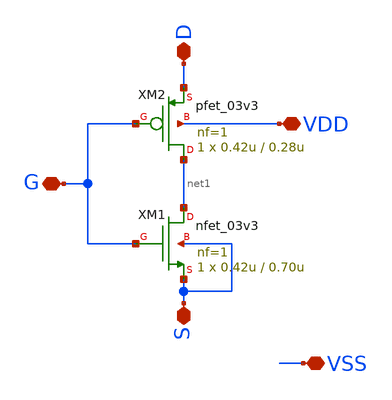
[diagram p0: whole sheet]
** sch_path: gf180mcuD/schematic/xschem/gf180_dnwell_inv.sch
**.subckt gf180_dnwell_inv S VSS D G VDD
*.iopin S
*.iopin VSS
*.iopin D
*.iopin G
*.iopin VDD
XM1 net1 G S S nfet_03v3 L=0.70u W=0.42u nf=1 ad='int((nf+1)/2) * W/nf * 0.18u' as='int((nf+2)/2) * W/nf * 0.18u'
+ pd='2*int((nf+1)/2) * (W/nf + 0.18u)' ps='2*int((nf+2)/2) * (W/nf + 0.18u)' nrd='0.18u / W' nrs='0.18u / W'
+ sa=0 sb=0 sd=0 m=1 par=1
XM2 net1 G D VDD pfet_03v3 L=0.28u W=0.42u nf=1 ad='int((nf+1)/2) * W/nf * 0.18u' as='int((nf+2)/2) * W/nf * 0.18u'
+ pd='2*int((nf+1)/2) * (W/nf + 0.18u)' ps='2*int((nf+2)/2) * (W/nf + 0.18u)' nrd='0.18u / W' nrs='0.18u / W'
+ sa=0 sb=0 sd=0 m=1 par=1
**.ends
.end
